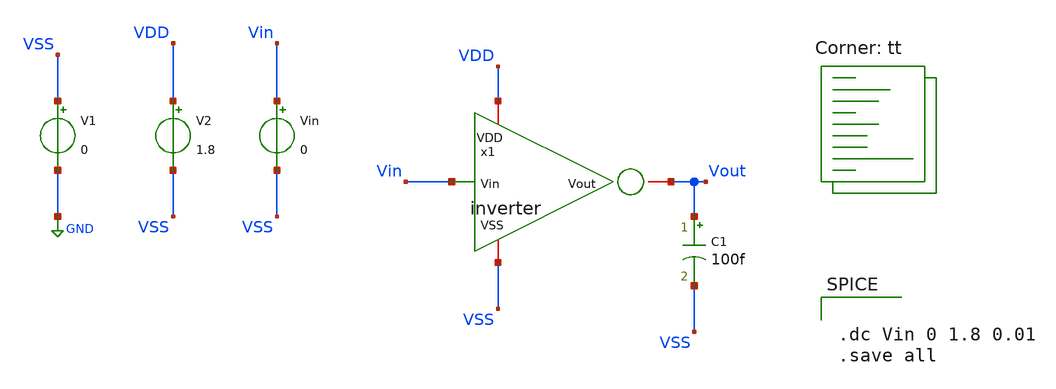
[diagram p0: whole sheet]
** sch_path: Modulo_Analogico/Lab2/inverter_tb.sch
**.subckt inverter_tb
C1 Vout VSS 100f m=1
V1 VSS GND 0
V2 VDD VSS 1.8
Vin Vin VSS 0
x1 Vin VDD VSS Vout inverter
**** begin user architecture code


.dc Vin 0 1.8 0.01
.save all


.lib $::SKYWATER_MODELS/sky130.lib.spice tt
**** end user architecture code
**.ends
.GLOBAL GND
.end
